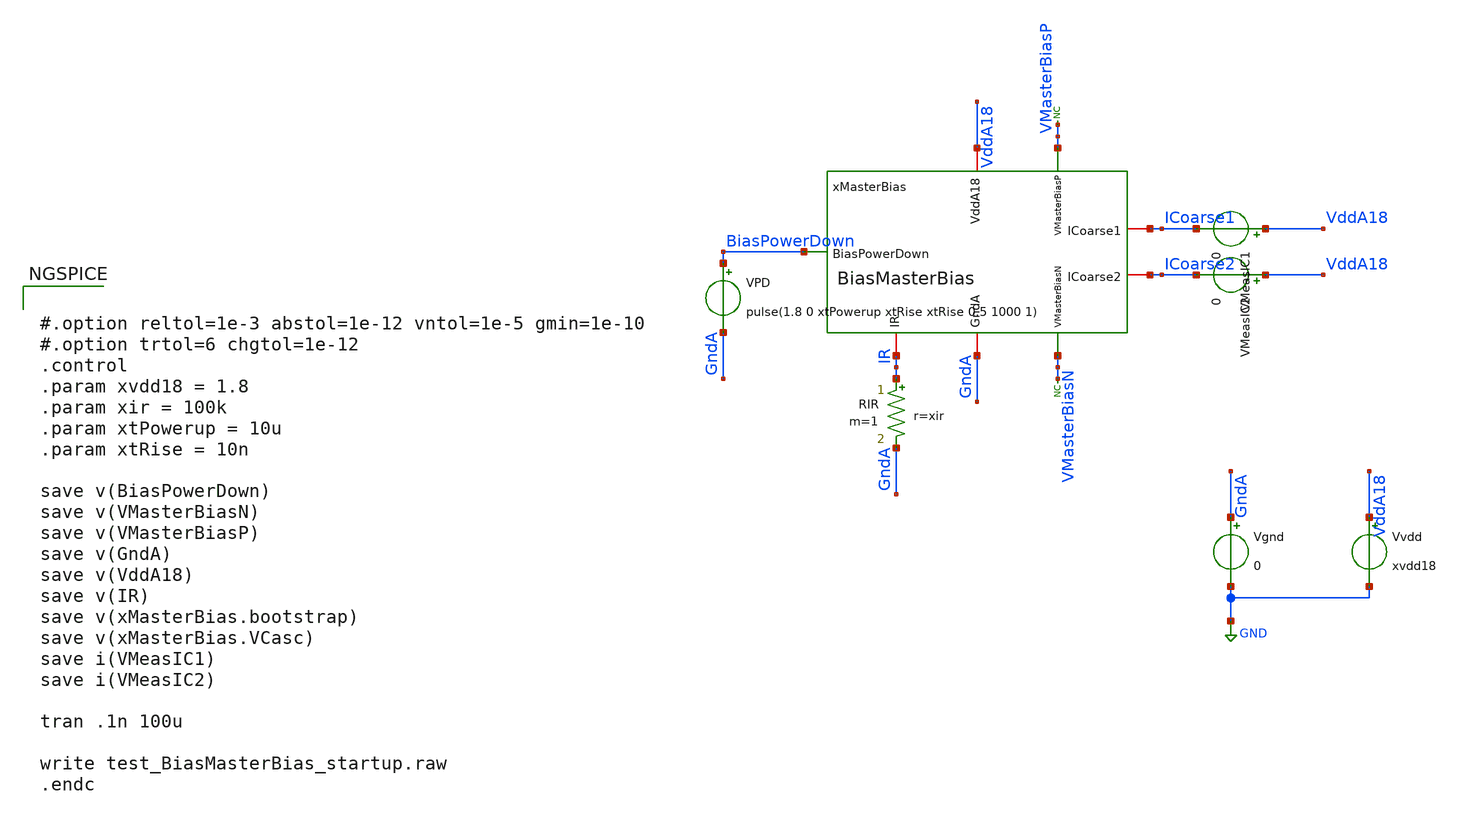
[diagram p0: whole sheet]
** sch_path: analog/xschem/test_BiasMasterBias.sch
**.subckt test_BiasMasterBias
xMasterBias VMasterBiasP ICoarse2 ICoarse1 VMasterBiasN BiasPowerDown VddA18 GndA IR BiasMasterBias
* noconn VMasterBiasP
* noconn VMasterBiasN
VMeasIC1 VddA18 ICoarse1 0
.save i(vmeasic1)
VMeasIC2 VddA18 ICoarse2 0
.save i(vmeasic2)
Vgnd GndA GND 0
.save i(vgnd)
Vvdd VddA18 GND xvdd18
.save i(vvdd)
RIR IR GndA r=xir m=1
VPD BiasPowerDown GndA pulse(1.8 0 xtPowerup xtRise xtRise 0.5 1000 1)
**** begin user architecture code

** opencircuitdesign pdks install
.lib $::SKYWATER_MODELS/sky130.lib.spice tt



#.option reltol=1e-3 abstol=1e-12 vntol=1e-5 gmin=1e-10
#.option trtol=6 chgtol=1e-12
.control
.param xvdd18 = 1.8
.param xir = 100k
.param xtPowerup = 10u
.param xtRise = 10n

save v(BiasPowerDown)
save v(VMasterBiasN)
save v(VMasterBiasP)
save v(GndA)
save v(VddA18)
save v(IR)
save v(xMasterBias.bootstrap)
save v(xMasterBias.VCasc)
save i(VMeasIC1)
save i(VMeasIC2)

tran .1n 100u

write test_BiasMasterBias_startup.raw
.endc


**** end user architecture code
**.ends

* expanding   symbol:  BiasMasterBias.sym # of pins=8
** sym_path: analog/xschem/BiasMasterBias.sym
** sch_path: analog/xschem/BiasMasterBias.sch
.subckt BiasMasterBias VMasterBiasP ICoarse2 ICoarse1 VMasterBiasN BiasPowerDown VddA18 GndA IR
*.opin VMasterBiasP
*.iopin IR
*.iopin VddA18
*.iopin GndA
*.opin VMasterBiasN
*.iopin ICoarse1
*.iopin ICoarse2
*.ipin BiasPowerDown
XMNBiasDio VMasterBiasN VMasterBiasN GndA GndA sky130_fd_pr__nfet_01v8_lvt L=5 W=20 nf=1 ad='int((1 + 1)/2) * 20 / 1 * 0.29'
+ as='int((1 + 2)/2) * 20 / 1 * 0.29' pd='2*int((1 + 1)/2) * (20 / 1 + 0.29)' ps='2*int((1 + 2)/2) * (20 / 1 + 0.29)'
+ nrd='0.29 / 20 ' nrs='0.29 / 20 ' sa=0 sb=0 sd=0 mult=12 m=12
XMPBias VCasc VMasterBiasP VddA18 VddA18 sky130_fd_pr__pfet_01v8 L=20 W=2 nf=1 ad='int((1 + 1)/2) * 2 / 1 * 0.29'
+ as='int((1 + 2)/2) * 2 / 1 * 0.29' pd='2*int((1 + 1)/2) * (2 / 1 + 0.29)' ps='2*int((1 + 2)/2) * (2 / 1 + 0.29)'
+ nrd='0.29 / 2 ' nrs='0.29 / 2 ' sa=0 sb=0 sd=0 mult=8 m=8
XMNBias net1 VMasterBiasN IR GndA sky130_fd_pr__nfet_01v8_lvt L=5 W=20 nf=1 ad='int((1 + 1)/2) * 20 / 1 * 0.29'
+ as='int((1 + 2)/2) * 20 / 1 * 0.29' pd='2*int((1 + 1)/2) * (20 / 1 + 0.29)' ps='2*int((1 + 2)/2) * (20 / 1 + 0.29)'
+ nrd='0.29 / 20 ' nrs='0.29 / 20 ' sa=0 sb=0 sd=0 mult=16 m=16
XMnBiasCascDio VCasc VCasc VMasterBiasN GndA sky130_fd_pr__nfet_01v8_lvt L=20 W=1 nf=1 ad='int((1 + 1)/2) * 1 / 1 * 0.29'
+ as='int((1 + 2)/2) * 1 / 1 * 0.29' pd='2*int((1 + 1)/2) * (1 / 1 + 0.29)' ps='2*int((1 + 2)/2) * (1 / 1 + 0.29)'
+ nrd='0.29 / 1 ' nrs='0.29 / 1 ' sa=0 sb=0 sd=0 mult=12 m=12
XMnBiasCasc VMasterBiasP VCasc net1 GndA sky130_fd_pr__nfet_01v8_lvt L=20 W=1 nf=1 ad='int((1 + 1)/2) * 1 / 1 * 0.29'
+ as='int((1 + 2)/2) * 1 / 1 * 0.29' pd='2*int((1 + 1)/2) * (1 / 1 + 0.29)' ps='2*int((1 + 2)/2) * (1 / 1 + 0.29)'
+ nrd='0.29 / 1 ' nrs='0.29 / 1 ' sa=0 sb=0 sd=0 mult=16 m=16
XMPBiasDio VMasterBiasP VMasterBiasP VddA18 VddA18 sky130_fd_pr__pfet_01v8 L=20 W=2 nf=1 ad='int((1 + 1)/2) * 2 / 1 * 0.29'
+ as='int((1 + 2)/2) * 2 / 1 * 0.29' pd='2*int((1 + 1)/2) * (2 / 1 + 0.29)' ps='2*int((1 + 2)/2) * (2 / 1 + 0.29)'
+ nrd='0.29 / 2 ' nrs='0.29 / 2 ' sa=0 sb=0 sd=0 mult=8 m=8
XMNMirr1 net2 VMasterBiasN GndA GndA sky130_fd_pr__nfet_01v8_lvt L=5 W=20 nf=1 ad='int((1 + 1)/2) * 20 / 1 * 0.29'
+ as='int((1 + 2)/2) * 20 / 1 * 0.29' pd='2*int((1 + 1)/2) * (20 / 1 + 0.29)' ps='2*int((1 + 2)/2) * (20 / 1 + 0.29)'
+ nrd='0.29 / 20 ' nrs='0.29 / 20 ' sa=0 sb=0 sd=0 mult=1 m=1
XMNMirrCasc1 ICoarse1 VCasc net2 GndA sky130_fd_pr__nfet_01v8_lvt L=20 W=1 nf=1 ad='int((1 + 1)/2) * 1 / 1 * 0.29'
+ as='int((1 + 2)/2) * 1 / 1 * 0.29' pd='2*int((1 + 1)/2) * (1 / 1 + 0.29)' ps='2*int((1 + 2)/2) * (1 / 1 + 0.29)'
+ nrd='0.29 / 1 ' nrs='0.29 / 1 ' sa=0 sb=0 sd=0 mult=1 m=1
XMNMirr2 net3 VMasterBiasN GndA GndA sky130_fd_pr__nfet_01v8_lvt L=5 W=20 nf=1 ad='int((1 + 1)/2) * 20 / 1 * 0.29'
+ as='int((1 + 2)/2) * 20 / 1 * 0.29' pd='2*int((1 + 1)/2) * (20 / 1 + 0.29)' ps='2*int((1 + 2)/2) * (20 / 1 + 0.29)'
+ nrd='0.29 / 20 ' nrs='0.29 / 20 ' sa=0 sb=0 sd=0 mult=1 m=1
XMNMirrCasc2 ICoarse2 VCasc net3 GndA sky130_fd_pr__nfet_01v8_lvt L=20 W=1 nf=1 ad='int((1 + 1)/2) * 1 / 1 * 0.29'
+ as='int((1 + 2)/2) * 1 / 1 * 0.29' pd='2*int((1 + 1)/2) * (1 / 1 + 0.29)' ps='2*int((1 + 2)/2) * (1 / 1 + 0.29)'
+ nrd='0.29 / 1 ' nrs='0.29 / 1 ' sa=0 sb=0 sd=0 mult=1 m=1
XMNBSPD VCasc BiasPowerDown GndA GndA sky130_fd_pr__nfet_01v8_lvt L=0.2 W=2 nf=1 ad='int((1 + 1)/2) * 2 / 1 * 0.29'
+ as='int((1 + 2)/2) * 2 / 1 * 0.29' pd='2*int((1 + 1)/2) * (2 / 1 + 0.29)' ps='2*int((1 + 2)/2) * (2 / 1 + 0.29)'
+ nrd='0.29 / 2 ' nrs='0.29 / 2 ' sa=0 sb=0 sd=0 mult=1 m=1
XMNBSCapBias VddA18 VMasterBiasP VddA18 GndA sky130_fd_pr__nfet_01v8 L=16 W=16 nf=1 ad='int((1 + 1)/2) * 16 / 1 * 0.29'
+ as='int((1 + 2)/2) * 16 / 1 * 0.29' pd='2*int((1 + 1)/2) * (16 / 1 + 0.29)' ps='2*int((1 + 2)/2) * (16 / 1 + 0.29)'
+ nrd='0.29 / 16 ' nrs='0.29 / 16 ' sa=0 sb=0 sd=0 mult=1 m=1
XMPBS bootstrap VMasterBiasP VddA18 VddA18 sky130_fd_pr__pfet_01v8 L=0.2 W=2 nf=1 ad='int((1 + 1)/2) * 2 / 1 * 0.29'
+ as='int((1 + 2)/2) * 2 / 1 * 0.29' pd='2*int((1 + 1)/2) * (2 / 1 + 0.29)' ps='2*int((1 + 2)/2) * (2 / 1 + 0.29)'
+ nrd='0.29 / 2 ' nrs='0.29 / 2 ' sa=0 sb=0 sd=0 mult=1 m=1
XMNBSCapBS BiasPowerDown bootstrap BiasPowerDown GndA sky130_fd_pr__nfet_01v8 L=16 W=16 nf=1 ad='int((1 + 1)/2) * 16 / 1 * 0.29'
+ as='int((1 + 2)/2) * 16 / 1 * 0.29' pd='2*int((1 + 1)/2) * (16 / 1 + 0.29)' ps='2*int((1 + 2)/2) * (16 / 1 + 0.29)'
+ nrd='0.29 / 16 ' nrs='0.29 / 16 ' sa=0 sb=0 sd=0 mult=1 m=1
XMPBSPU VCasc bootstrap VddA18 VddA18 sky130_fd_pr__pfet_01v8 L=0.2 W=2 nf=1 ad='int((1 + 1)/2) * 2 / 1 * 0.29'
+ as='int((1 + 2)/2) * 2 / 1 * 0.29' pd='2*int((1 + 1)/2) * (2 / 1 + 0.29)' ps='2*int((1 + 2)/2) * (2 / 1 + 0.29)'
+ nrd='0.29 / 2 ' nrs='0.29 / 2 ' sa=0 sb=0 sd=0 mult=1 m=1
.ends

.GLOBAL GND
.end
